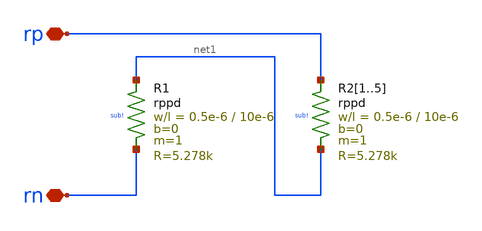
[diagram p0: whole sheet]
** sch_path: xschem/bandgap_simple_res-6k.sch
* (c) 2025 H. Pretl, Apache-2.0 license
**.subckt bandgap_simple_res-6k rp rn
*.iopin rp
*.iopin rn
XR1 net1 rn sub! rppd w=0.5e-6 l=10e-6 m=1 b=0 mm_ok=1
XR21 rp net1 sub! rppd w=0.5e-6 l=10e-6 m=1 b=0 mm_ok=1
XR22 rp net1 sub! rppd w=0.5e-6 l=10e-6 m=1 b=0 mm_ok=1
XR23 rp net1 sub! rppd w=0.5e-6 l=10e-6 m=1 b=0 mm_ok=1
XR24 rp net1 sub! rppd w=0.5e-6 l=10e-6 m=1 b=0 mm_ok=1
XR25 rp net1 sub! rppd w=0.5e-6 l=10e-6 m=1 b=0 mm_ok=1
**.ends
.end
